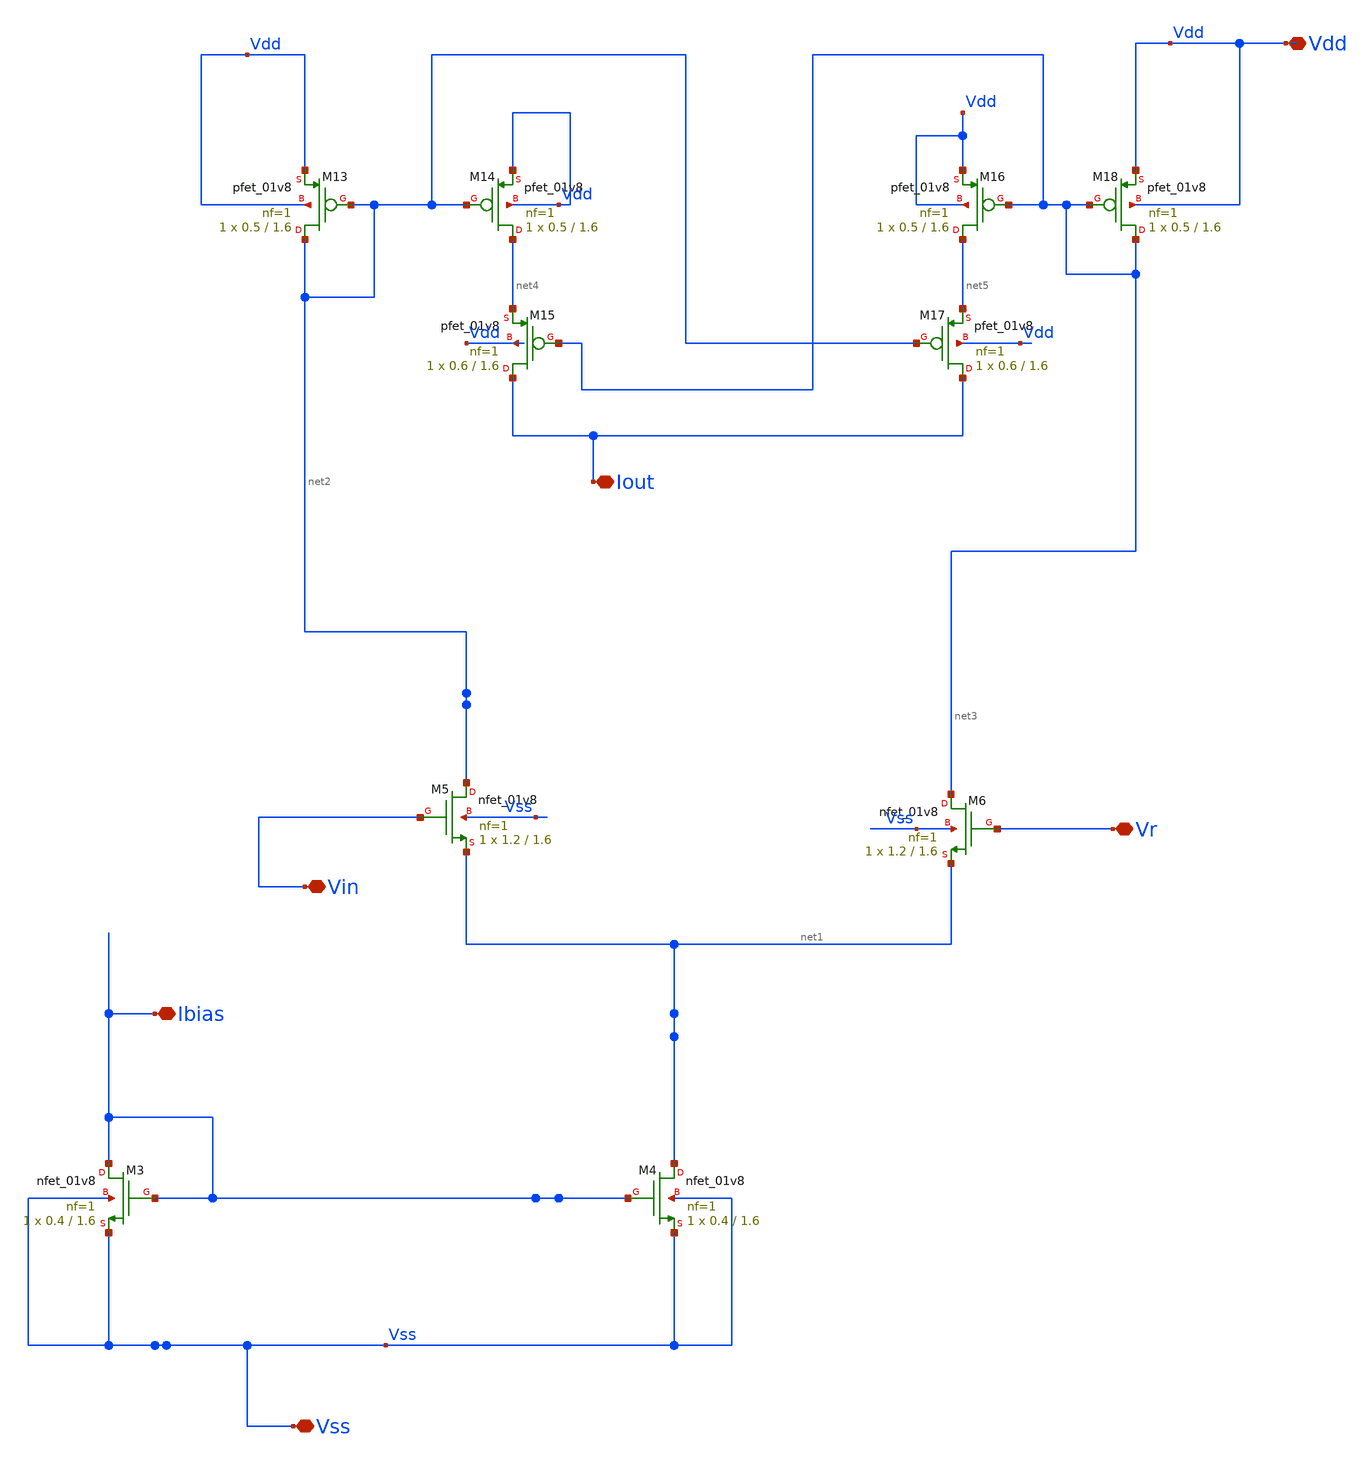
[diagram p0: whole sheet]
** sch_path: xschem/bump_final_tt.sch
**.subckt bump_final_tt Vss Vin Vr Ibias Iout Vdd
*.iopin Vss
*.iopin Vin
*.iopin Vr
*.iopin Ibias
*.iopin Iout
*.iopin Vdd
XM3 Ibias Ibias Vss Vss sky130_fd_pr__nfet_01v8 L=1.6 W=0.4 nf=1 ad='int((1 + 1)/2) * 0.4 / 1 * 0.29'
+ as='int((1 + 2)/2) * 0.4 / 1 * 0.29' pd='2*int((1 + 1)/2) * (0.4 / 1 + 0.29)' ps='2*int((1 + 2)/2) * (0.4 / 1 + 0.29)'
+ nrd='0.29 / 0.4 ' nrs='0.29 / 0.4 ' sa=0 sb=0 sd=0 mult=1 m=1
XM4 net1 Ibias Vss Vss sky130_fd_pr__nfet_01v8 L=1.6 W=0.4 nf=1 ad='int((1 + 1)/2) * 0.4 / 1 * 0.29'
+ as='int((1 + 2)/2) * 0.4 / 1 * 0.29' pd='2*int((1 + 1)/2) * (0.4 / 1 + 0.29)' ps='2*int((1 + 2)/2) * (0.4 / 1 + 0.29)'
+ nrd='0.29 / 0.4 ' nrs='0.29 / 0.4 ' sa=0 sb=0 sd=0 mult=1 m=1
XM5 net2 Vin net1 Vss sky130_fd_pr__nfet_01v8 L=1.6 W=1.2 nf=1 ad='int((1 + 1)/2) * 1.2 / 1 * 0.29' as='int((1 + 2)/2) * 1.2 / 1 * 0.29'
+ pd='2*int((1 + 1)/2) * (1.2 / 1 + 0.29)' ps='2*int((1 + 2)/2) * (1.2 / 1 + 0.29)' nrd='0.29 / 1.2 ' nrs='0.29 / 1.2 '
+ sa=0 sb=0 sd=0 mult=1 m=1
XM6 net3 Vr net1 Vss sky130_fd_pr__nfet_01v8 L=1.6 W=1.2 nf=1 ad='int((1 + 1)/2) * 1.2 / 1 * 0.29' as='int((1 + 2)/2) * 1.2 / 1 * 0.29'
+ pd='2*int((1 + 1)/2) * (1.2 / 1 + 0.29)' ps='2*int((1 + 2)/2) * (1.2 / 1 + 0.29)' nrd='0.29 / 1.2 ' nrs='0.29 / 1.2 '
+ sa=0 sb=0 sd=0 mult=1 m=1
XM13 net2 net2 Vdd Vdd sky130_fd_pr__pfet_01v8 L=1.6 W=0.5 nf=1 ad='int((nf+1)/2) * W/nf * 0.29' as='int((nf+2)/2) * W/nf * 0.29'
+ pd='2*int((nf+1)/2) * (W/nf + 0.29)' ps='2*int((nf+2)/2) * (W/nf + 0.29)' nrd='0.29 / W' nrs='0.29 / W'
+ sa=0 sb=0 sd=0 mult=1 m=1
XM14 net4 net2 Vdd Vdd sky130_fd_pr__pfet_01v8 L=1.6 W=0.5 nf=1 ad='int((nf+1)/2) * W/nf * 0.29' as='int((nf+2)/2) * W/nf * 0.29'
+ pd='2*int((nf+1)/2) * (W/nf + 0.29)' ps='2*int((nf+2)/2) * (W/nf + 0.29)' nrd='0.29 / W' nrs='0.29 / W'
+ sa=0 sb=0 sd=0 mult=1 m=1
XM15 Iout net3 net4 Vdd sky130_fd_pr__pfet_01v8 L=1.6 W=0.6 nf=1 ad='int((nf+1)/2) * W/nf * 0.29' as='int((nf+2)/2) * W/nf * 0.29'
+ pd='2*int((nf+1)/2) * (W/nf + 0.29)' ps='2*int((nf+2)/2) * (W/nf + 0.29)' nrd='0.29 / W' nrs='0.29 / W'
+ sa=0 sb=0 sd=0 mult=1 m=1
XM16 net5 net3 Vdd Vdd sky130_fd_pr__pfet_01v8 L=1.6 W=0.5 nf=1 ad='int((nf+1)/2) * W/nf * 0.29' as='int((nf+2)/2) * W/nf * 0.29'
+ pd='2*int((nf+1)/2) * (W/nf + 0.29)' ps='2*int((nf+2)/2) * (W/nf + 0.29)' nrd='0.29 / W' nrs='0.29 / W'
+ sa=0 sb=0 sd=0 mult=1 m=1
XM17 Iout net2 net5 Vdd sky130_fd_pr__pfet_01v8 L=1.6 W=0.6 nf=1 ad='int((nf+1)/2) * W/nf * 0.29' as='int((nf+2)/2) * W/nf * 0.29'
+ pd='2*int((nf+1)/2) * (W/nf + 0.29)' ps='2*int((nf+2)/2) * (W/nf + 0.29)' nrd='0.29 / W' nrs='0.29 / W'
+ sa=0 sb=0 sd=0 mult=1 m=1
XM18 net3 net3 Vdd Vdd sky130_fd_pr__pfet_01v8 L=1.6 W=0.5 nf=1 ad='int((nf+1)/2) * W/nf * 0.29' as='int((nf+2)/2) * W/nf * 0.29'
+ pd='2*int((nf+1)/2) * (W/nf + 0.29)' ps='2*int((nf+2)/2) * (W/nf + 0.29)' nrd='0.29 / W' nrs='0.29 / W'
+ sa=0 sb=0 sd=0 mult=1 m=1
**.ends
.end
